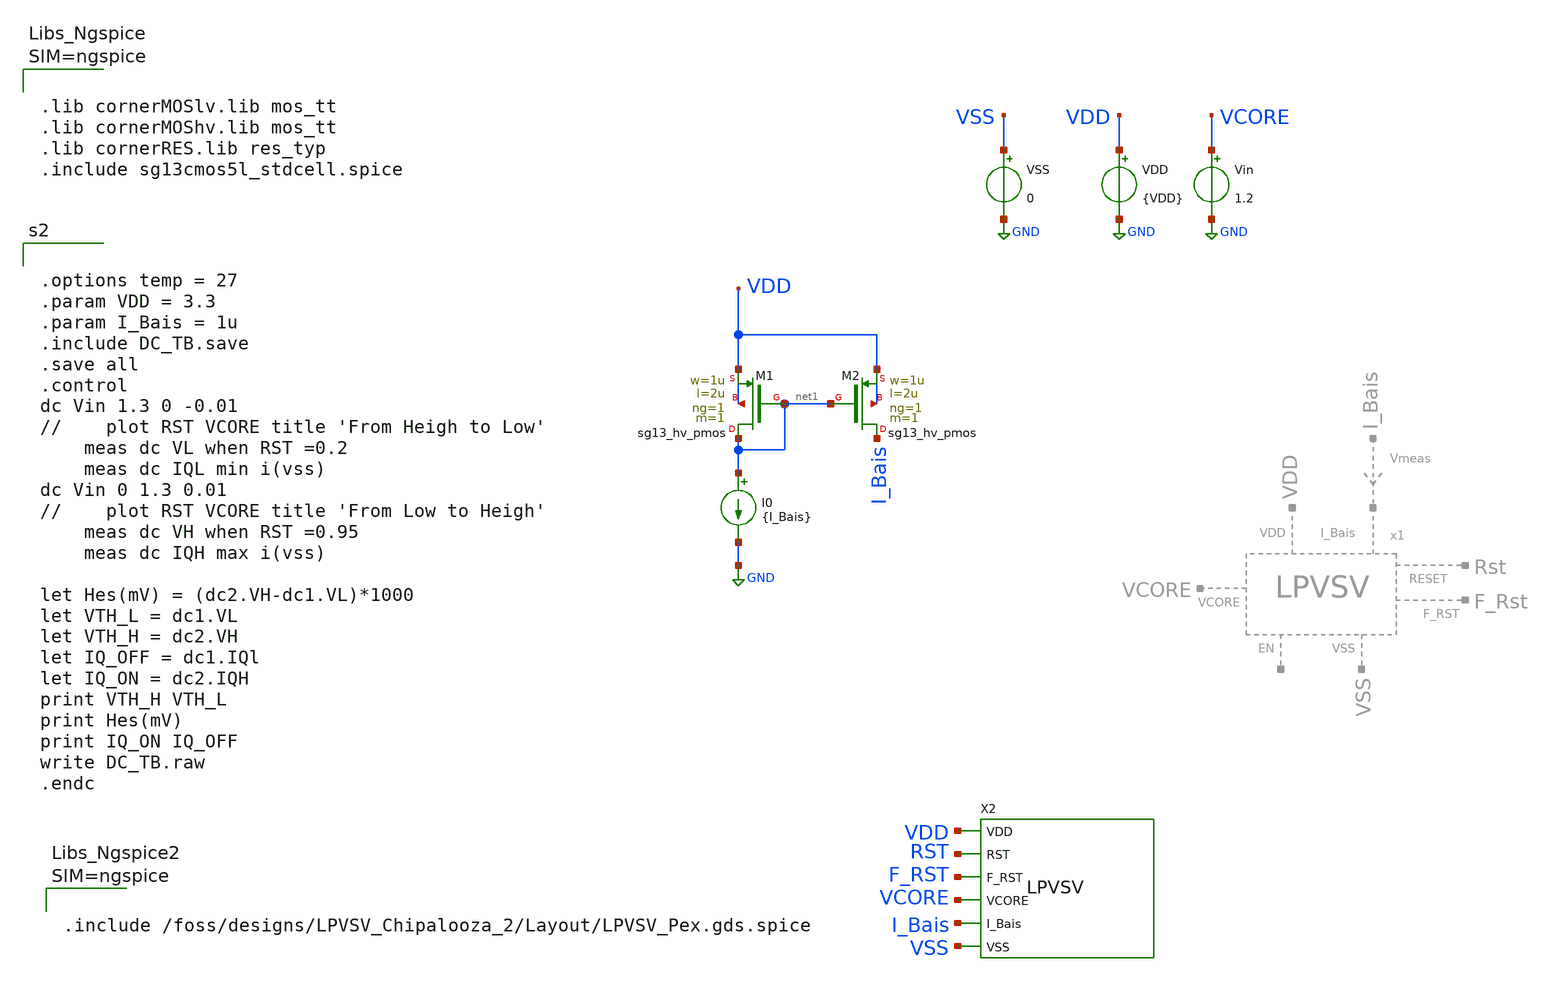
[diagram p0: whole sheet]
** sch_path: Simulation/DC_TB.sch
**.subckt DC_TB
VDD VDD GND {VDD}
VSS VSS GND 0
Vin VCORE GND 1.2
I0 net1 GND {I_Bais}
X2 VSS F_RST VDD VCORE I_Bais RST LPVSV
XM1 net1 net1 VDD VDD sg13_hv_pmos w=1u l=2u ng=1 m=1 mm_ok=1
XM2 I_Bais net1 VDD VDD sg13_hv_pmos w=1u l=2u ng=1 m=1 mm_ok=1
**** begin user architecture code


.options temp = 27
.param VDD = 3.3
.param I_Bais = 1u
.include DC_TB.save
.save all
.control
dc Vin 1.3 0 -0.01
//	plot RST VCORE title 'From Heigh to Low'
	meas dc VL when RST =0.2
	meas dc IQL min i(vss)
dc Vin 0 1.3 0.01
//	plot RST VCORE title 'From Low to Heigh'
	meas dc VH when RST =0.95
	meas dc IQH max i(vss)

let Hes(mV) = (dc2.VH-dc1.VL)*1000
let VTH_L = dc1.VL
let VTH_H = dc2.VH
let IQ_OFF = dc1.IQl
let IQ_ON = dc2.IQH
print VTH_H VTH_L
print Hes(mV)
print IQ_ON IQ_OFF
write DC_TB.raw
.endc




.options rshunt = 1e15
.options gmin=1e-9
.options reltol = 0.01 abstol = 1p
.option filetype=ascii





.lib cornerMOSlv.lib mos_tt
.lib cornerMOShv.lib mos_tt
.lib cornerRES.lib res_typ
.include sg13cmos5l_stdcell.spice






.include /foss/designs/LPVSV_Chipalooza_2/Layout/LPVSV_Pex.gds.spice



**** end user architecture code
**.ends
.GLOBAL GND
.end
